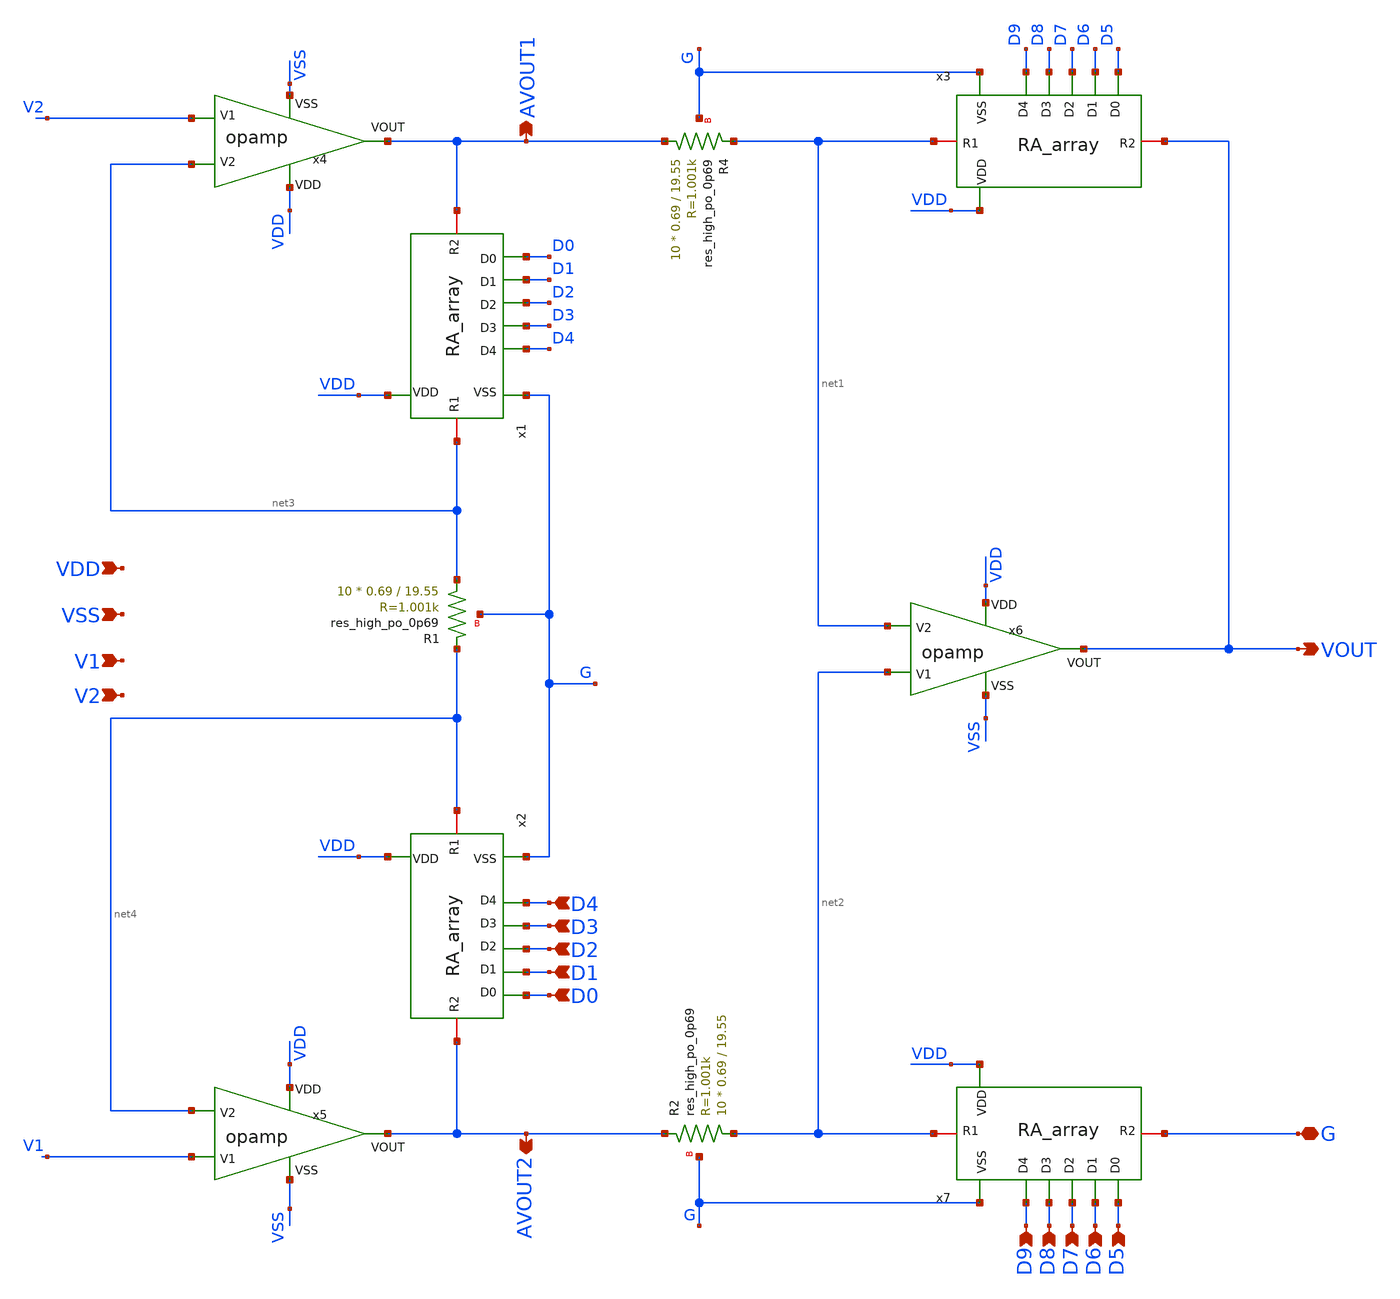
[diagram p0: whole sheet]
** sch_path: IA_v2.sch
**.subckt IA_v2 VOUT G VDD VSS V1 V2 D4 D3 D2 D1 D0 D9 D8 D7 D6 D5 AVOUT1 AVOUT2
*.opin VOUT
*.iopin G
*.ipin VDD
*.ipin VSS
*.ipin V1
*.ipin V2
*.ipin D4
*.ipin D3
*.ipin D2
*.ipin D1
*.ipin D0
*.ipin D9
*.ipin D8
*.ipin D7
*.ipin D6
*.ipin D5
*.opin AVOUT1
*.opin AVOUT2
x4 VDD VSS V2 net3 AVOUT1 opamp
x5 VDD VSS V1 net4 AVOUT2 opamp
x6 VDD VSS net2 net1 VOUT opamp
x1 G net3 AVOUT1 D0 D1 D2 D3 D4 VDD RA_array
x2 G net4 AVOUT2 D0 D1 D2 D3 D4 VDD RA_array
x3 G net1 VOUT D5 D6 D7 D8 D9 VDD RA_array
x7 G net2 G D5 D6 D7 D8 D9 VDD RA_array
XR4 AVOUT1 net1 G sky130_fd_pr__res_high_po_0p69 L=19.55 mult=10 m=10
XR1 net3 net4 G sky130_fd_pr__res_high_po_0p69 L=19.55 mult=10 m=10
XR2 net2 AVOUT2 G sky130_fd_pr__res_high_po_0p69 L=19.55 mult=10 m=10
**.ends
.end
